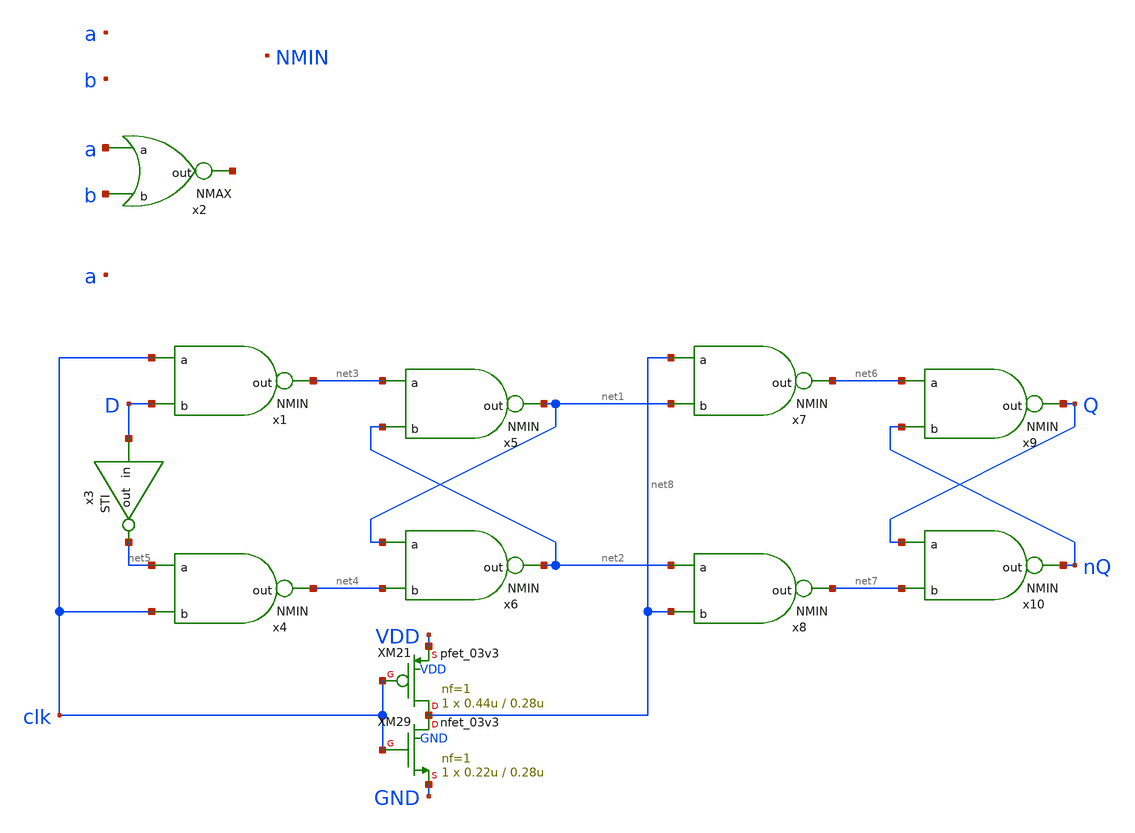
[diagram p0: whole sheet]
** sch_path: xschem_designs/untitled.sch
**.subckt untitled
x1 net3 clk D NMIN
x2 net9 a b NMAX
x3 D net5 STI
x4 net4 net5 clk NMIN
x5 net1 net3 net2 NMIN
x6 net2 net1 net4 NMIN
x7 net6 net8 net1 NMIN
x8 net7 net2 net8 NMIN
x9 Q net6 nQ NMIN
x10 nQ Q net7 NMIN
XM21 net8 clk VDD VDD pfet_03v3 L=0.28u W=0.44u nf=1 ad='int((nf+1)/2) * W/nf * 0.18u' as='int((nf+2)/2) * W/nf * 0.18u'
+ pd='2*int((nf+1)/2) * (W/nf + 0.18u)' ps='2*int((nf+2)/2) * (W/nf + 0.18u)' nrd='0.18u / W' nrs='0.18u / W'
+ sa=0 sb=0 sd=0 m=1 par=1
XM29 net8 clk GND GND nfet_03v3 L=0.28u W=0.22u nf=1 ad='int((nf+1)/2) * W/nf * 0.18u' as='int((nf+2)/2) * W/nf * 0.18u'
+ pd='2*int((nf+1)/2) * (W/nf + 0.18u)' ps='2*int((nf+2)/2) * (W/nf + 0.18u)' nrd='0.18u / W' nrs='0.18u / W'
+ sa=0 sb=0 sd=0 m=1 par=1
**.ends

* expanding   symbol:  xschem_designs/NMIN.sym # of pins=3
** sym_path: xschem_designs/NMIN.sym
** sch_path: xschem_designs/NMIN.sch
.subckt NMIN out a b
*.ipin a
*.ipin b
*.opin out
XM21 net1 a VDD VDD pfet_03v3 L=0.28u W=0.44u nf=1 ad='int((nf+1)/2) * W/nf * 0.18u' as='int((nf+2)/2) * W/nf * 0.18u'
+ pd='2*int((nf+1)/2) * (W/nf + 0.18u)' ps='2*int((nf+2)/2) * (W/nf + 0.18u)' nrd='0.18u / W' nrs='0.18u / W'
+ sa=0 sb=0 sd=0 m=1 par=1
XM22 out out net1 VDD pfet_03v3 L=2.24u W=0.44u nf=1 ad='int((nf+1)/2) * W/nf * 0.18u' as='int((nf+2)/2) * W/nf * 0.18u'
+ pd='2*int((nf+1)/2) * (W/nf + 0.18u)' ps='2*int((nf+2)/2) * (W/nf + 0.18u)' nrd='0.18u / W' nrs='0.18u / W'
+ sa=0 sb=0 sd=0 m=1 par=1
XM23 out a VDD BP pfet_06v0 L=1.1u W=0.60u nf=1 ad='int((nf+1)/2) * W/nf * 0.18u' as='int((nf+2)/2) * W/nf * 0.18u'
+ pd='2*int((nf+1)/2) * (W/nf + 0.18u)' ps='2*int((nf+2)/2) * (W/nf + 0.18u)' nrd='0.18u / W' nrs='0.18u / W'
+ sa=0 sb=0 sd=0 m=1 par=1
XM24 out b VDD BP pfet_06v0 L=1.1u W=0.60u nf=1 ad='int((nf+1)/2) * W/nf * 0.18u' as='int((nf+2)/2) * W/nf * 0.18u'
+ pd='2*int((nf+1)/2) * (W/nf + 0.18u)' ps='2*int((nf+2)/2) * (W/nf + 0.18u)' nrd='0.18u / W' nrs='0.18u / W'
+ sa=0 sb=0 sd=0 m=1 par=1
XM25 net1 b VDD VDD pfet_03v3 L=0.28u W=0.44u nf=1 ad='int((nf+1)/2) * W/nf * 0.18u' as='int((nf+2)/2) * W/nf * 0.18u'
+ pd='2*int((nf+1)/2) * (W/nf + 0.18u)' ps='2*int((nf+2)/2) * (W/nf + 0.18u)' nrd='0.18u / W' nrs='0.18u / W'
+ sa=0 sb=0 sd=0 m=1 par=1
XM26 out out net2 GND nfet_03v3 L=2.24u W=0.22u nf=1 ad='int((nf+1)/2) * W/nf * 0.18u' as='int((nf+2)/2) * W/nf * 0.18u'
+ pd='2*int((nf+1)/2) * (W/nf + 0.18u)' ps='2*int((nf+2)/2) * (W/nf + 0.18u)' nrd='0.18u / W' nrs='0.18u / W'
+ sa=0 sb=0 sd=0 m=1 par=1
XM27 net3 a GND BN nfet_06v0 L=1.4u W=0.30u nf=1 ad='int((nf+1)/2) * W/nf * 0.18u' as='int((nf+2)/2) * W/nf * 0.18u'
+ pd='2*int((nf+1)/2) * (W/nf + 0.18u)' ps='2*int((nf+2)/2) * (W/nf + 0.18u)' nrd='0.18u / W' nrs='0.18u / W'
+ sa=0 sb=0 sd=0 m=1 par=1
XM28 out b net3 BN nfet_06v0 L=1.4u W=0.30u nf=1 ad='int((nf+1)/2) * W/nf * 0.18u' as='int((nf+2)/2) * W/nf * 0.18u'
+ pd='2*int((nf+1)/2) * (W/nf + 0.18u)' ps='2*int((nf+2)/2) * (W/nf + 0.18u)' nrd='0.18u / W' nrs='0.18u / W'
+ sa=0 sb=0 sd=0 m=1 par=1
XM29 net4 a GND GND nfet_03v3 L=0.28u W=0.22u nf=1 ad='int((nf+1)/2) * W/nf * 0.18u' as='int((nf+2)/2) * W/nf * 0.18u'
+ pd='2*int((nf+1)/2) * (W/nf + 0.18u)' ps='2*int((nf+2)/2) * (W/nf + 0.18u)' nrd='0.18u / W' nrs='0.18u / W'
+ sa=0 sb=0 sd=0 m=1 par=1
XM30 net2 b net4 GND nfet_03v3 L=0.28u W=0.22u nf=1 ad='int((nf+1)/2) * W/nf * 0.18u' as='int((nf+2)/2) * W/nf * 0.18u'
+ pd='2*int((nf+1)/2) * (W/nf + 0.18u)' ps='2*int((nf+2)/2) * (W/nf + 0.18u)' nrd='0.18u / W' nrs='0.18u / W'
+ sa=0 sb=0 sd=0 m=1 par=1
.ends


* expanding   symbol:  xschem_designs/NMAX.sym # of pins=3
** sym_path: xschem_designs/NMAX.sym
** sch_path: xschem_designs/NMAX.sch
.subckt NMAX out a b
*.ipin a
*.ipin b
*.opin out
XM13 out out net1 GND nfet_03v3 L=2.24u W=0.22u nf=1 ad='int((nf+1)/2) * W/nf * 0.18u' as='int((nf+2)/2) * W/nf * 0.18u'
+ pd='2*int((nf+1)/2) * (W/nf + 0.18u)' ps='2*int((nf+2)/2) * (W/nf + 0.18u)' nrd='0.18u / W' nrs='0.18u / W'
+ sa=0 sb=0 sd=0 m=1 par=1
XM14 out a GND BN nfet_06v0 L=1.4u W=0.30u nf=1 ad='int((nf+1)/2) * W/nf * 0.18u' as='int((nf+2)/2) * W/nf * 0.18u'
+ pd='2*int((nf+1)/2) * (W/nf + 0.18u)' ps='2*int((nf+2)/2) * (W/nf + 0.18u)' nrd='0.18u / W' nrs='0.18u / W'
+ sa=0 sb=0 sd=0 m=1 par=1
XM15 out b GND BN nfet_06v0 L=1.4u W=0.30u nf=1 ad='int((nf+1)/2) * W/nf * 0.18u' as='int((nf+2)/2) * W/nf * 0.18u'
+ pd='2*int((nf+1)/2) * (W/nf + 0.18u)' ps='2*int((nf+2)/2) * (W/nf + 0.18u)' nrd='0.18u / W' nrs='0.18u / W'
+ sa=0 sb=0 sd=0 m=1 par=1
XM18 net1 a GND GND nfet_03v3 L=0.28u W=0.22u nf=1 ad='int((nf+1)/2) * W/nf * 0.18u' as='int((nf+2)/2) * W/nf * 0.18u'
+ pd='2*int((nf+1)/2) * (W/nf + 0.18u)' ps='2*int((nf+2)/2) * (W/nf + 0.18u)' nrd='0.18u / W' nrs='0.18u / W'
+ sa=0 sb=0 sd=0 m=1 par=1
XM19 net1 b GND GND nfet_03v3 L=0.28u W=0.22u nf=1 ad='int((nf+1)/2) * W/nf * 0.18u' as='int((nf+2)/2) * W/nf * 0.18u'
+ pd='2*int((nf+1)/2) * (W/nf + 0.18u)' ps='2*int((nf+2)/2) * (W/nf + 0.18u)' nrd='0.18u / W' nrs='0.18u / W'
+ sa=0 sb=0 sd=0 m=1 par=1
XM11 net2 a VDD VDD pfet_03v3 L=0.28u W=0.44u nf=1 ad='int((nf+1)/2) * W/nf * 0.18u' as='int((nf+2)/2) * W/nf * 0.18u'
+ pd='2*int((nf+1)/2) * (W/nf + 0.18u)' ps='2*int((nf+2)/2) * (W/nf + 0.18u)' nrd='0.18u / W' nrs='0.18u / W'
+ sa=0 sb=0 sd=0 m=1 par=1
XM12 out out net3 VDD pfet_03v3 L=1.12u W=0.22u nf=1 ad='int((nf+1)/2) * W/nf * 0.18u' as='int((nf+2)/2) * W/nf * 0.18u'
+ pd='2*int((nf+1)/2) * (W/nf + 0.18u)' ps='2*int((nf+2)/2) * (W/nf + 0.18u)' nrd='0.18u / W' nrs='0.18u / W'
+ sa=0 sb=0 sd=0 m=1 par=1
XM16 net4 a VDD BP pfet_06v0 L=1.1u W=0.60u nf=1 ad='int((nf+1)/2) * W/nf * 0.18u' as='int((nf+2)/2) * W/nf * 0.18u'
+ pd='2*int((nf+1)/2) * (W/nf + 0.18u)' ps='2*int((nf+2)/2) * (W/nf + 0.18u)' nrd='0.18u / W' nrs='0.18u / W'
+ sa=0 sb=0 sd=0 m=1 par=1
XM17 out b net4 BP pfet_06v0 L=1.1u W=0.60u nf=1 ad='int((nf+1)/2) * W/nf * 0.18u' as='int((nf+2)/2) * W/nf * 0.18u'
+ pd='2*int((nf+1)/2) * (W/nf + 0.18u)' ps='2*int((nf+2)/2) * (W/nf + 0.18u)' nrd='0.18u / W' nrs='0.18u / W'
+ sa=0 sb=0 sd=0 m=1 par=1
XM20 net3 b net2 VDD pfet_03v3 L=0.28u W=0.44u nf=1 ad='int((nf+1)/2) * W/nf * 0.18u' as='int((nf+2)/2) * W/nf * 0.18u'
+ pd='2*int((nf+1)/2) * (W/nf + 0.18u)' ps='2*int((nf+2)/2) * (W/nf + 0.18u)' nrd='0.18u / W' nrs='0.18u / W'
+ sa=0 sb=0 sd=0 m=1 par=1
.ends


* expanding   symbol:  xschem_designs/STI.sym # of pins=2
** sym_path: xschem_designs/STI.sym
** sch_path: xschem_designs/STI.sch
.subckt STI in out
*.ipin in
*.opin out
XM225 out out net1 GND nfet_03v3 L=2.24u W=0.22u nf=1 ad='int((nf+1)/2) * W/nf * 0.18u' as='int((nf+2)/2) * W/nf * 0.18u'
+ pd='2*int((nf+1)/2) * (W/nf + 0.18u)' ps='2*int((nf+2)/2) * (W/nf + 0.18u)' nrd='0.18u / W' nrs='0.18u / W'
+ sa=0 sb=0 sd=0 m=1 par=1
XM226 out out net2 VDD pfet_03v3 L=1.12u W=0.22u nf=1 ad='int((nf+1)/2) * W/nf * 0.18u' as='int((nf+2)/2) * W/nf * 0.18u'
+ pd='2*int((nf+1)/2) * (W/nf + 0.18u)' ps='2*int((nf+2)/2) * (W/nf + 0.18u)' nrd='0.18u / W' nrs='0.18u / W'
+ sa=0 sb=0 sd=0 m=1 par=1
XM237 net2 in VDD VDD pfet_03v3 L=0.28u W=0.44u nf=1 ad='int((nf+1)/2) * W/nf * 0.18u' as='int((nf+2)/2) * W/nf * 0.18u'
+ pd='2*int((nf+1)/2) * (W/nf + 0.18u)' ps='2*int((nf+2)/2) * (W/nf + 0.18u)' nrd='0.18u / W' nrs='0.18u / W'
+ sa=0 sb=0 sd=0 m=1 par=1
XM238 net1 in GND GND nfet_03v3 L=0.28u W=0.22u nf=1 ad='int((nf+1)/2) * W/nf * 0.18u' as='int((nf+2)/2) * W/nf * 0.18u'
+ pd='2*int((nf+1)/2) * (W/nf + 0.18u)' ps='2*int((nf+2)/2) * (W/nf + 0.18u)' nrd='0.18u / W' nrs='0.18u / W'
+ sa=0 sb=0 sd=0 m=1 par=1
XM241 out in VDD BP pfet_06v0 L=1.1u W=0.60u nf=1 ad='int((nf+1)/2) * W/nf * 0.18u' as='int((nf+2)/2) * W/nf * 0.18u'
+ pd='2*int((nf+1)/2) * (W/nf + 0.18u)' ps='2*int((nf+2)/2) * (W/nf + 0.18u)' nrd='0.18u / W' nrs='0.18u / W'
+ sa=0 sb=0 sd=0 m=1 par=1
XM242 out in GND BN nfet_06v0 L=1.4u W=0.30u nf=1 ad='int((nf+1)/2) * W/nf * 0.18u' as='int((nf+2)/2) * W/nf * 0.18u'
+ pd='2*int((nf+1)/2) * (W/nf + 0.18u)' ps='2*int((nf+2)/2) * (W/nf + 0.18u)' nrd='0.18u / W' nrs='0.18u / W'
+ sa=0 sb=0 sd=0 m=1 par=1
.ends

.end
